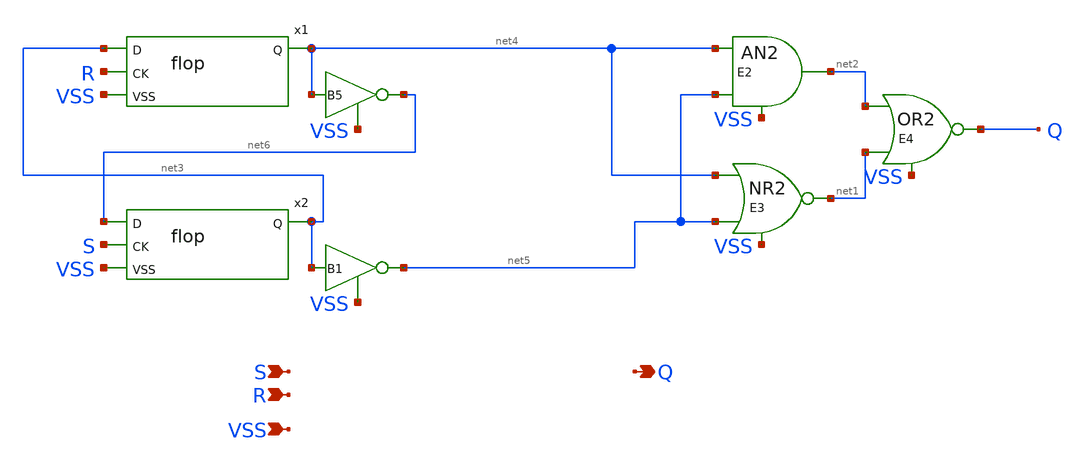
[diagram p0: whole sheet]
** sch_path: tests/test_sweep_diff/examples/sr_flop/schematic/sr_flop.sch
* Copyright (C) 1998-2024 Stefan Frederik Schippers
* This program is free software; you can redistribute it and/or modify
* it under the terms of the GNU General Public License as published by
* the Free Software Foundation; either version 2 of the License, or
* (at your option) any later version.
* This program is distributed in the hope that it will be useful,
* but WITHOUT ANY WARRANTY; without even the implied warranty of
* MERCHANTABILITY or FITNESS FOR A PARTICULAR PURPOSE.  See the
* GNU General Public License for more details.
* You should have received a copy of the GNU General Public License
* along with this program; if not, write to the Free Software
**.subckt sr_flop S Q VSS R
*.ipin S
*.opin Q
*.ipin VSS
*.ipin R
x1 net3 net4 R VSS flop VTH=VTH VHI=VHI
x2 net6 net3 S VSS flop VTH=VTH VHI=VHI
E2 net2 VSS and(2) net4 VSS net5 VSS 'VTH-0.1' 0.0 'VTH+0.1' VHI
E3 net1 VSS nor(2) net4 VSS net5 VSS 'VTH-0.1' VHI 'VTH+0.1' 0.0
E4 Q VSS or(2) net2 VSS net1 VSS 'VTH-0.1' 0.0 'VTH+0.1' VHI
B5 net6 VSS V=pwl(v( net4 , VSS ), 'VTH-0.1' VHI 'VTH+0.1' 0 )
B1 net5 VSS V=pwl(v( net3 , VSS ), 'VTH-0.1' VHI 'VTH+0.1' 0 )
**.ends
.end
